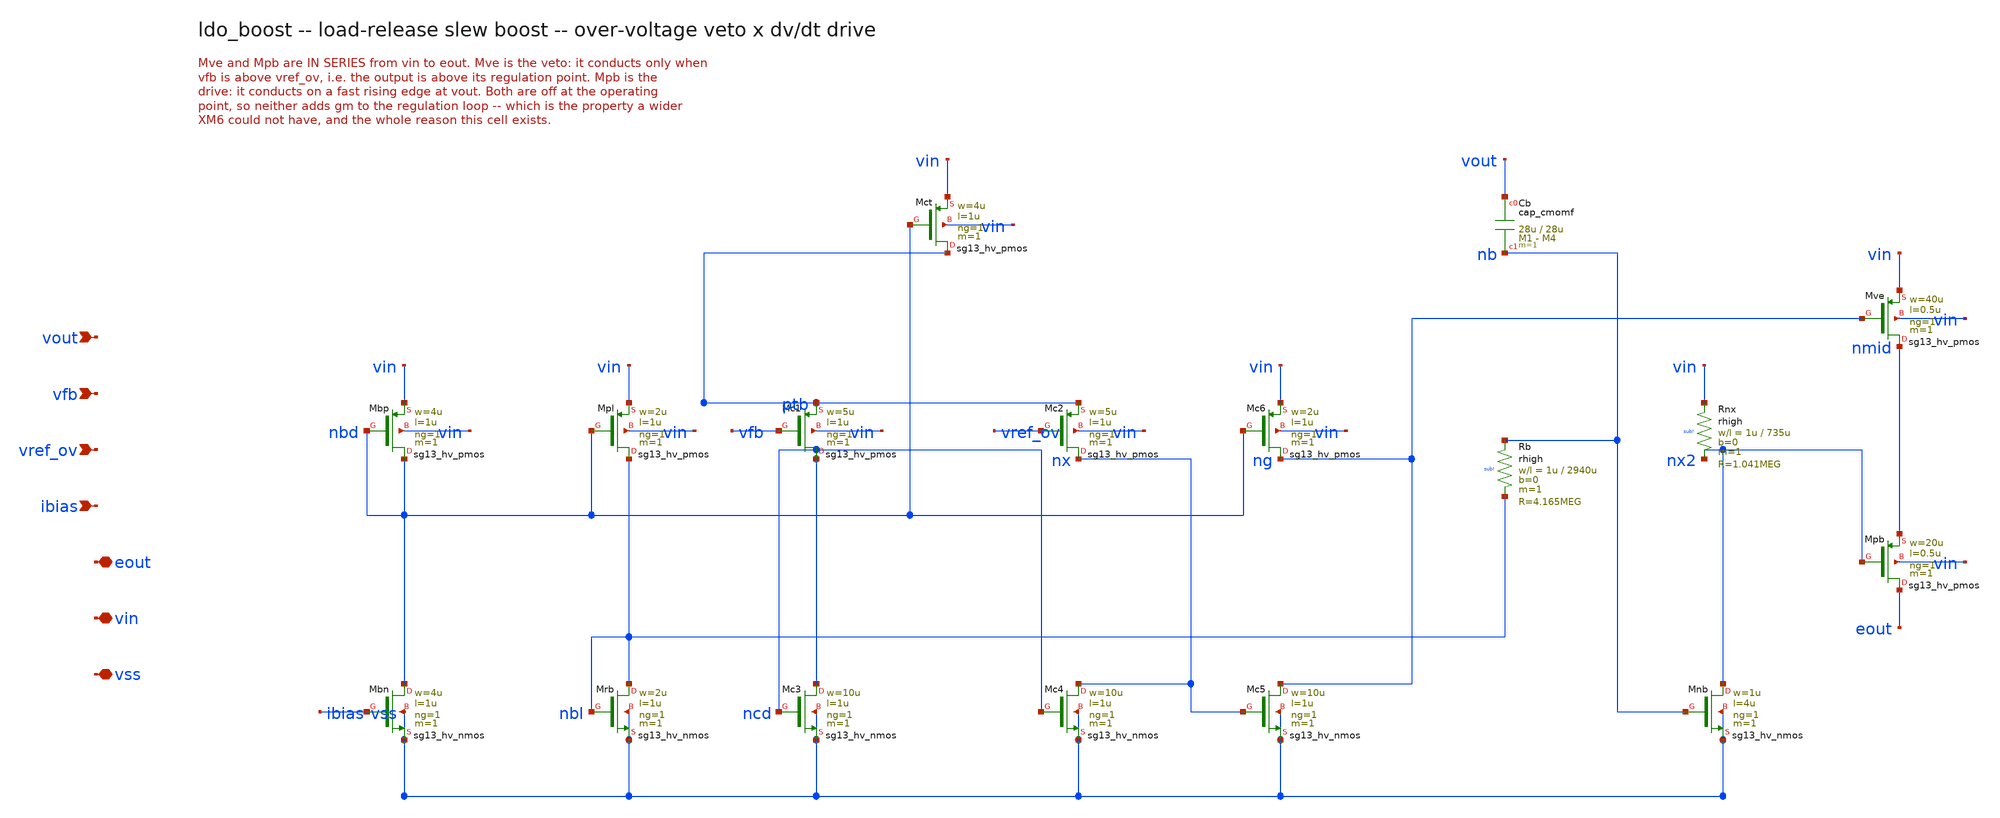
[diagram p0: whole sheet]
** sch_path: xschem/ldo_boost_wired.sch
**.subckt ldo_boost_wired vout vfb vref_ov ibias eout vin vss
*.ipin vout
*.ipin vfb
*.ipin vref_ov
*.ipin ibias
*.iopin eout
*.iopin vin
*.iopin vss
XMbn nbd ibias vss vss sg13_hv_nmos w=4u l=1u ng=1 m=1 mm_ok=1
XMbp nbd nbd vin vin sg13_hv_pmos w=4u l=1u ng=1 m=1 mm_ok=1
XMpl nbl nbd vin vin sg13_hv_pmos w=2u l=1u ng=1 m=1 mm_ok=1
XMrb nbl nbl vss vss sg13_hv_nmos w=2u l=1u ng=1 m=1 mm_ok=1
XMct ptb nbd vin vin sg13_hv_pmos w=4u l=1u ng=1 m=1 mm_ok=1
XMc1 ncd vfb ptb vin sg13_hv_pmos w=5u l=1u ng=1 m=1 mm_ok=1
XMc2 nx vref_ov ptb vin sg13_hv_pmos w=5u l=1u ng=1 m=1 mm_ok=1
XMc3 ncd ncd vss vss sg13_hv_nmos w=10u l=1u ng=1 m=1 mm_ok=1
XMc4 nx ncd vss vss sg13_hv_nmos w=10u l=1u ng=1 m=1 mm_ok=1
XMc6 ng nbd vin vin sg13_hv_pmos w=2u l=1u ng=1 m=1 mm_ok=1
XMc5 ng nx vss vss sg13_hv_nmos w=10u l=1u ng=1 m=1 mm_ok=1
XCb vout nb cap_cmomf w=28u l=28u mmin=1 mmax=4 subblock=0 rfmodel=0 subscale=1 m=1 mm_ok=1
XRb nb nbl sub! rhigh w=1u l=2940u m=1 b=0 mm_ok=1
XMnb nx2 nb vss vss sg13_hv_nmos w=1u l=4u ng=1 m=1 mm_ok=1
XRnx vin nx2 sub! rhigh w=1u l=735u m=1 b=0 mm_ok=1
XMve nmid ng vin vin sg13_hv_pmos w=40u l=0.5u ng=1 m=1 mm_ok=1
XMpb eout nx2 nmid vin sg13_hv_pmos w=20u l=0.5u ng=1 m=1 mm_ok=1
**.ends
.end
